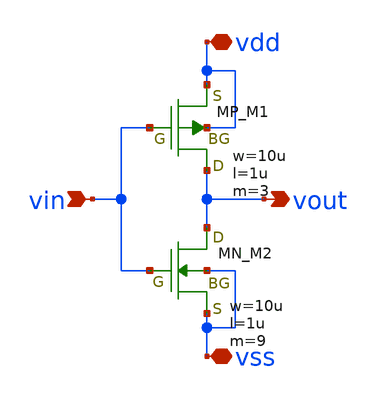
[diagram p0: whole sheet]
** sch_path: member_project/DCDC/xschem/inverter_sw.sch
**.subckt inverter_sw vin vdd vss vout
*.ipin vin
*.iopin vdd
*.iopin vss
*.opin vout
XM1 vout vin vdd vdd PMOS w=10u l=1u as=0 ad=0 ps=0 pd=0 nrd=0 nrs=0 m=3
XM2 vout vin vss vss NMOS w=10u l=1u as=0 ad=0 ps=0 pd=0 nrd=0 nrs=0 m=9
**.ends
.end
